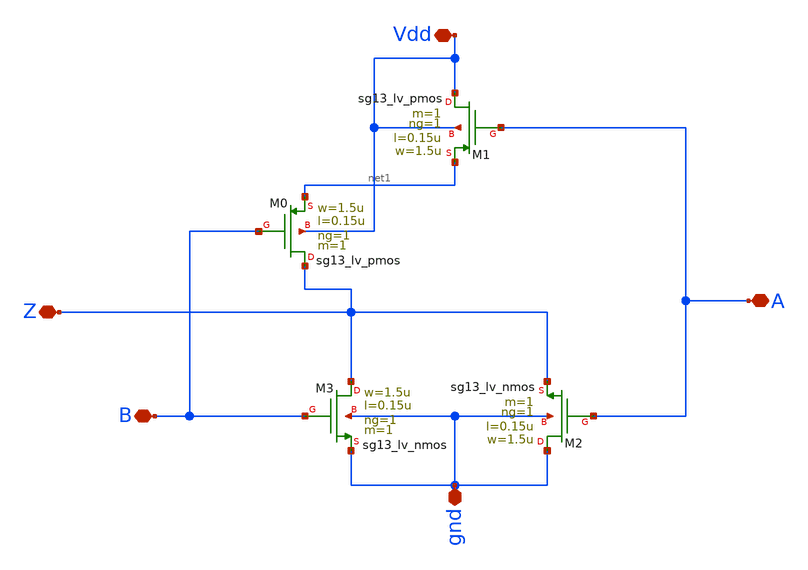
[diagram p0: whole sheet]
** sch_path: design/blocks/nor/schematic/nor.sch
**.subckt nor A B Vdd Z gnd
*.iopin A
*.iopin B
*.iopin Vdd
*.iopin Z
*.iopin gnd
XM2 gnd A Z gnd sg13_lv_nmos w=1.5u l=0.15u ng=1 m=1 mm_ok=1
XM3 Z B gnd gnd sg13_lv_nmos w=1.5u l=0.15u ng=1 m=1 mm_ok=1
XM0 Z B net1 Vdd sg13_lv_pmos w=1.5u l=0.15u ng=1 m=1 mm_ok=1
XM1 Vdd A net1 Vdd sg13_lv_pmos w=1.5u l=0.15u ng=1 m=1 mm_ok=1
**.ends
.end
